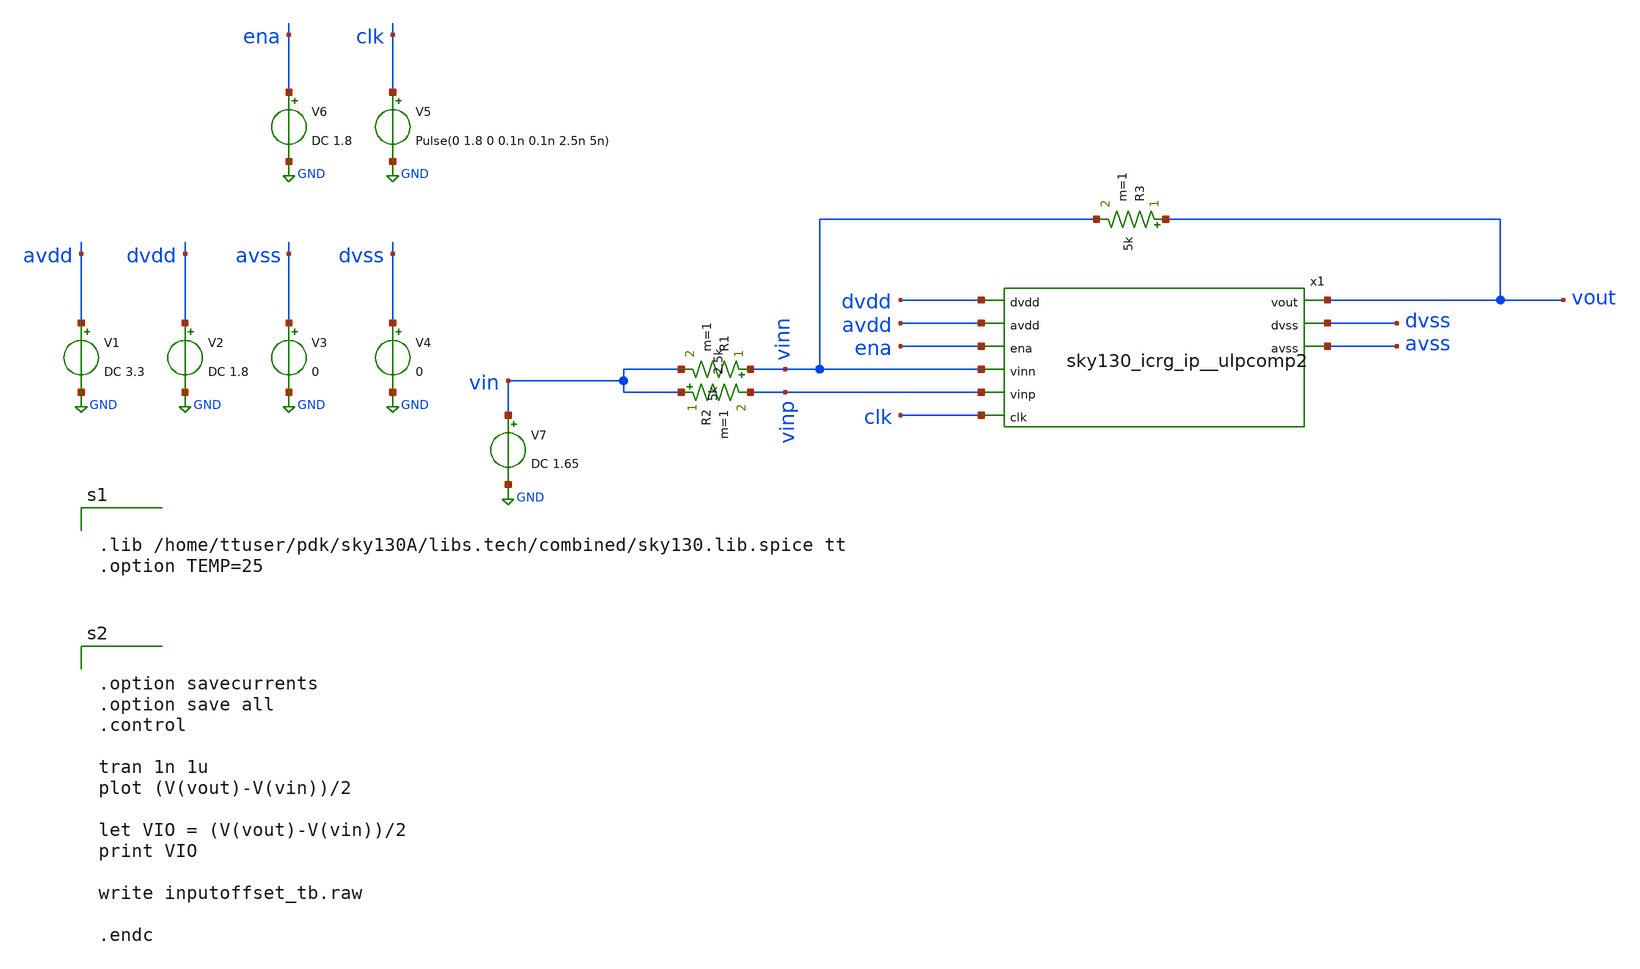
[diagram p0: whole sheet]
** sch_path: xschem/inputoffset_tb.sch
**.subckt inputoffset_tb
x1 dvdd avdd ena vout vinn vinp clk dvss avss sky130_icrg_ip__ulpcomp2
V1 avdd GND DC 3.3
V2 dvdd GND DC 1.8
V3 avss GND 0
V4 dvss GND 0
V5 clk GND Pulse(0 1.8 0 0.1n 0.1n 2.5n 5n)
V6 ena GND DC 1.8
V7 vin GND DC 1.65
R1 vinn vin 5k m=1
R2 vin vinp 2.5k m=1
R3 vout vinn 5k m=1
**** begin user architecture code


.lib /home/ttuser/pdk/sky130A/libs.tech/combined/sky130.lib.spice tt
.option TEMP=25



.option savecurrents
.option save all
.control

tran 1n 1u
plot (V(vout)-V(vin))/2

let VIO = (V(vout)-V(vin))/2
print VIO

write inputoffset_tb.raw

.endc

**** end user architecture code
**.ends

* expanding   symbol:  sky130_icrg_ip__ulpcomp2.sym # of pins=9
** sym_path: xschem/sky130_icrg_ip__ulpcomp2.sym
** sch_path: xschem/sky130_icrg_ip__ulpcomp2.sch
.subckt sky130_icrg_ip__ulpcomp2 dvdd avdd ena vout vinn vinp clk dvss avss
*.ipin avdd
*.ipin vinp
*.ipin vinn
*.opin avss
*.opin vout
*.opin dvss
*.ipin dvdd
*.ipin clk
*.ipin ena
XM2 oneg vinp net1 net1 sky130_fd_pr__pfet_g5v0d10v5 L=1 W=5 nf=1 ad='int((nf+1)/2) * W/nf * 0.29' as='int((nf+2)/2) * W/nf * 0.29'
+ pd='2*int((nf+1)/2) * (W/nf + 0.29)' ps='2*int((nf+2)/2) * (W/nf + 0.29)' nrd='0.29 / W' nrs='0.29 / W'
+ sa=0 sb=0 sd=0 mult=1 m=1
XM3 opos vinn net1 net1 sky130_fd_pr__pfet_g5v0d10v5 L=1 W=5 nf=1 ad='int((nf+1)/2) * W/nf * 0.29' as='int((nf+2)/2) * W/nf * 0.29'
+ pd='2*int((nf+1)/2) * (W/nf + 0.29)' ps='2*int((nf+2)/2) * (W/nf + 0.29)' nrd='0.29 / W' nrs='0.29 / W'
+ sa=0 sb=0 sd=0 mult=1 m=1
XM7 oneg clka net2 net2 sky130_fd_pr__nfet_03v3_nvt L=0.5 W=3 nf=1 ad='int((nf+1)/2) * W/nf * 0.29' as='int((nf+2)/2) * W/nf * 0.29'
+ pd='2*int((nf+1)/2) * (W/nf + 0.29)' ps='2*int((nf+2)/2) * (W/nf + 0.29)' nrd='0.29 / W' nrs='0.29 / W'
+ sa=0 sb=0 sd=0 mult=1 m=1
XM5 opos clka net2 net2 sky130_fd_pr__nfet_03v3_nvt L=0.5 W=3 nf=1 ad='int((nf+1)/2) * W/nf * 0.29' as='int((nf+2)/2) * W/nf * 0.29'
+ pd='2*int((nf+1)/2) * (W/nf + 0.29)' ps='2*int((nf+2)/2) * (W/nf + 0.29)' nrd='0.29 / W' nrs='0.29 / W'
+ sa=0 sb=0 sd=0 mult=1 m=1
XM4 net2 net2 avss avss sky130_fd_pr__nfet_03v3_nvt L=0.5 W=3 nf=1 ad='int((nf+1)/2) * W/nf * 0.29' as='int((nf+2)/2) * W/nf * 0.29'
+ pd='2*int((nf+1)/2) * (W/nf + 0.29)' ps='2*int((nf+2)/2) * (W/nf + 0.29)' nrd='0.29 / W' nrs='0.29 / W'
+ sa=0 sb=0 sd=0 mult=1 m=1
XM18 vout net4 dvss dvss sky130_fd_pr__nfet_01v8 L=0.5 W=1 nf=1 ad='int((nf+1)/2) * W/nf * 0.29' as='int((nf+2)/2) * W/nf * 0.29'
+ pd='2*int((nf+1)/2) * (W/nf + 0.29)' ps='2*int((nf+2)/2) * (W/nf + 0.29)' nrd='0.29 / W' nrs='0.29 / W'
+ sa=0 sb=0 sd=0 mult=1 m=1
XM19 vout net4 dvddb dvddb sky130_fd_pr__pfet_01v8 L=1 W=2 nf=1 ad='int((nf+1)/2) * W/nf * 0.29' as='int((nf+2)/2) * W/nf * 0.29'
+ pd='2*int((nf+1)/2) * (W/nf + 0.29)' ps='2*int((nf+2)/2) * (W/nf + 0.29)' nrd='0.29 / W' nrs='0.29 / W'
+ sa=0 sb=0 sd=0 mult=1 m=1
XM22 clka clkb dvddb dvddb sky130_fd_pr__pfet_01v8 L=0.5 W=2 nf=1 ad='int((nf+1)/2) * W/nf * 0.29' as='int((nf+2)/2) * W/nf * 0.29'
+ pd='2*int((nf+1)/2) * (W/nf + 0.29)' ps='2*int((nf+2)/2) * (W/nf + 0.29)' nrd='0.29 / W' nrs='0.29 / W'
+ sa=0 sb=0 sd=0 mult=1 m=1
XM20 net3 enab avdd avdd sky130_fd_pr__pfet_g5v0d10v5 L=1 W=5 nf=1 ad='int((nf+1)/2) * W/nf * 0.29' as='int((nf+2)/2) * W/nf * 0.29'
+ pd='2*int((nf+1)/2) * (W/nf + 0.29)' ps='2*int((nf+2)/2) * (W/nf + 0.29)' nrd='0.29 / W' nrs='0.29 / W'
+ sa=0 sb=0 sd=0 mult=1 m=1
XM8 clkb clk dvddb dvddb sky130_fd_pr__pfet_01v8 L=0.5 W=2 nf=1 ad='int((nf+1)/2) * W/nf * 0.29' as='int((nf+2)/2) * W/nf * 0.29'
+ pd='2*int((nf+1)/2) * (W/nf + 0.29)' ps='2*int((nf+2)/2) * (W/nf + 0.29)' nrd='0.29 / W' nrs='0.29 / W'
+ sa=0 sb=0 sd=0 mult=1 m=1
XM25 enab ena dvdd dvdd sky130_fd_pr__pfet_01v8 L=0.5 W=2 nf=1 ad='int((nf+1)/2) * W/nf * 0.29' as='int((nf+2)/2) * W/nf * 0.29'
+ pd='2*int((nf+1)/2) * (W/nf + 0.29)' ps='2*int((nf+2)/2) * (W/nf + 0.29)' nrd='0.29 / W' nrs='0.29 / W'
+ sa=0 sb=0 sd=0 mult=1 m=1
XM13 net4 opos net6 dvss sky130_fd_pr__nfet_03v3_nvt L=0.5 W=2 nf=1 ad='int((nf+1)/2) * W/nf * 0.29'
+ as='int((nf+2)/2) * W/nf * 0.29' pd='2*int((nf+1)/2) * (W/nf + 0.29)' ps='2*int((nf+2)/2) * (W/nf + 0.29)'
+ nrd='0.29 / W' nrs='0.29 / W' sa=0 sb=0 sd=0 mult=1 m=1
XM14 net7 net4 net8 dvss sky130_fd_pr__nfet_03v3_nvt L=0.5 W=2 nf=1 ad='int((nf+1)/2) * W/nf * 0.29'
+ as='int((nf+2)/2) * W/nf * 0.29' pd='2*int((nf+1)/2) * (W/nf + 0.29)' ps='2*int((nf+2)/2) * (W/nf + 0.29)'
+ nrd='0.29 / W' nrs='0.29 / W' sa=0 sb=0 sd=0 mult=1 m=1
XM15 net8 clkb dvss dvss sky130_fd_pr__nfet_03v3_nvt L=0.5 W=2 nf=1 ad='int((nf+1)/2) * W/nf * 0.29'
+ as='int((nf+2)/2) * W/nf * 0.29' pd='2*int((nf+1)/2) * (W/nf + 0.29)' ps='2*int((nf+2)/2) * (W/nf + 0.29)'
+ nrd='0.29 / W' nrs='0.29 / W' sa=0 sb=0 sd=0 mult=1 m=1
XM16 net6 net5 net8 dvss sky130_fd_pr__nfet_03v3_nvt L=0.5 W=2 nf=1 ad='int((nf+1)/2) * W/nf * 0.29'
+ as='int((nf+2)/2) * W/nf * 0.29' pd='2*int((nf+1)/2) * (W/nf + 0.29)' ps='2*int((nf+2)/2) * (W/nf + 0.29)'
+ nrd='0.29 / W' nrs='0.29 / W' sa=0 sb=0 sd=0 mult=1 m=1
XM17 net5 oneg net7 dvss sky130_fd_pr__nfet_03v3_nvt L=0.5 W=2 nf=1 ad='int((nf+1)/2) * W/nf * 0.29'
+ as='int((nf+2)/2) * W/nf * 0.29' pd='2*int((nf+1)/2) * (W/nf + 0.29)' ps='2*int((nf+2)/2) * (W/nf + 0.29)'
+ nrd='0.29 / W' nrs='0.29 / W' sa=0 sb=0 sd=0 mult=1 m=1
XM6 clkb clk dvss dvss sky130_fd_pr__nfet_01v8 L=0.5 W=1 nf=1 ad='int((nf+1)/2) * W/nf * 0.29' as='int((nf+2)/2) * W/nf * 0.29'
+ pd='2*int((nf+1)/2) * (W/nf + 0.29)' ps='2*int((nf+2)/2) * (W/nf + 0.29)' nrd='0.29 / W' nrs='0.29 / W'
+ sa=0 sb=0 sd=0 mult=1 m=1
XM21 clka clkb dvss dvss sky130_fd_pr__nfet_01v8 L=0.5 W=1 nf=1 ad='int((nf+1)/2) * W/nf * 0.29' as='int((nf+2)/2) * W/nf * 0.29'
+ pd='2*int((nf+1)/2) * (W/nf + 0.29)' ps='2*int((nf+2)/2) * (W/nf + 0.29)' nrd='0.29 / W' nrs='0.29 / W'
+ sa=0 sb=0 sd=0 mult=1 m=1
XM24 enab ena dvss dvss sky130_fd_pr__nfet_01v8 L=0.5 W=1 nf=1 ad='int((nf+1)/2) * W/nf * 0.29' as='int((nf+2)/2) * W/nf * 0.29'
+ pd='2*int((nf+1)/2) * (W/nf + 0.29)' ps='2*int((nf+2)/2) * (W/nf + 0.29)' nrd='0.29 / W' nrs='0.29 / W'
+ sa=0 sb=0 sd=0 mult=1 m=1
XM1 net1 clka net3 net3 sky130_fd_pr__pfet_g5v0d10v5 L=1 W=5 nf=1 ad='int((nf+1)/2) * W/nf * 0.29' as='int((nf+2)/2) * W/nf * 0.29'
+ pd='2*int((nf+1)/2) * (W/nf + 0.29)' ps='2*int((nf+2)/2) * (W/nf + 0.29)' nrd='0.29 / W' nrs='0.29 / W'
+ sa=0 sb=0 sd=0 mult=1 m=1
XM23 dvddb enab dvdd dvdd sky130_fd_pr__pfet_01v8_hvt L=0.15 W=1 nf=1 ad='int((nf+1)/2) * W/nf * 0.29'
+ as='int((nf+2)/2) * W/nf * 0.29' pd='2*int((nf+1)/2) * (W/nf + 0.29)' ps='2*int((nf+2)/2) * (W/nf + 0.29)'
+ nrd='0.29 / W' nrs='0.29 / W' sa=0 sb=0 sd=0 mult=1 m=1
XM9 net4 clkb dvddb dvddb sky130_fd_pr__pfet_01v8_hvt L=1 W=3 nf=1 ad='int((nf+1)/2) * W/nf * 0.29' as='int((nf+2)/2) * W/nf * 0.29'
+ pd='2*int((nf+1)/2) * (W/nf + 0.29)' ps='2*int((nf+2)/2) * (W/nf + 0.29)' nrd='0.29 / W' nrs='0.29 / W'
+ sa=0 sb=0 sd=0 mult=2 m=2
XM10 net5 net4 dvddb dvddb sky130_fd_pr__pfet_01v8_hvt L=1 W=3 nf=1 ad='int((nf+1)/2) * W/nf * 0.29'
+ as='int((nf+2)/2) * W/nf * 0.29' pd='2*int((nf+1)/2) * (W/nf + 0.29)' ps='2*int((nf+2)/2) * (W/nf + 0.29)'
+ nrd='0.29 / W' nrs='0.29 / W' sa=0 sb=0 sd=0 mult=2 m=2
XM11 net4 net5 dvddb dvddb sky130_fd_pr__pfet_01v8_hvt L=1 W=3 nf=1 ad='int((nf+1)/2) * W/nf * 0.29'
+ as='int((nf+2)/2) * W/nf * 0.29' pd='2*int((nf+1)/2) * (W/nf + 0.29)' ps='2*int((nf+2)/2) * (W/nf + 0.29)'
+ nrd='0.29 / W' nrs='0.29 / W' sa=0 sb=0 sd=0 mult=2 m=2
XM12 net5 clkb dvddb dvddb sky130_fd_pr__pfet_01v8_hvt L=1 W=3 nf=1 ad='int((nf+1)/2) * W/nf * 0.29'
+ as='int((nf+2)/2) * W/nf * 0.29' pd='2*int((nf+1)/2) * (W/nf + 0.29)' ps='2*int((nf+2)/2) * (W/nf + 0.29)'
+ nrd='0.29 / W' nrs='0.29 / W' sa=0 sb=0 sd=0 mult=2 m=2
.ends

.GLOBAL GND
.end
